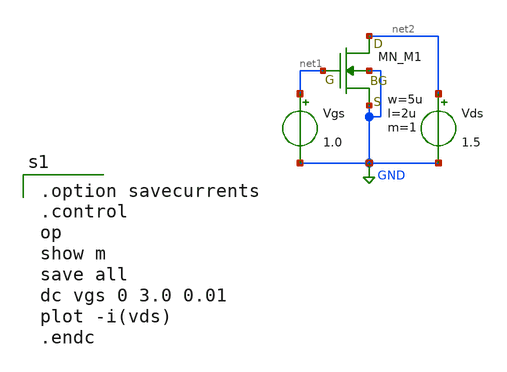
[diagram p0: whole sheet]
** sch_path: member_project/DCDC/ShuntaroOHNO/xschem/nmos_id.sch
**.subckt nmos_id
Vgs net1 GND 1.0
XM1 net2 net1 GND GND NMOS w=5u l=2u as=0 ad=0 ps=0 pd=0 nrd=0 nrs=0 m=1
Vds net2 GND 1.5
**** begin user architecture code
 .include $::LIB/ip62_models

.option savecurrents
.control
op
show m
save all
dc vgs 0 3.0 0.01
plot -i(vds)
.endc

**** end user architecture code
**.ends
.GLOBAL GND
.end
